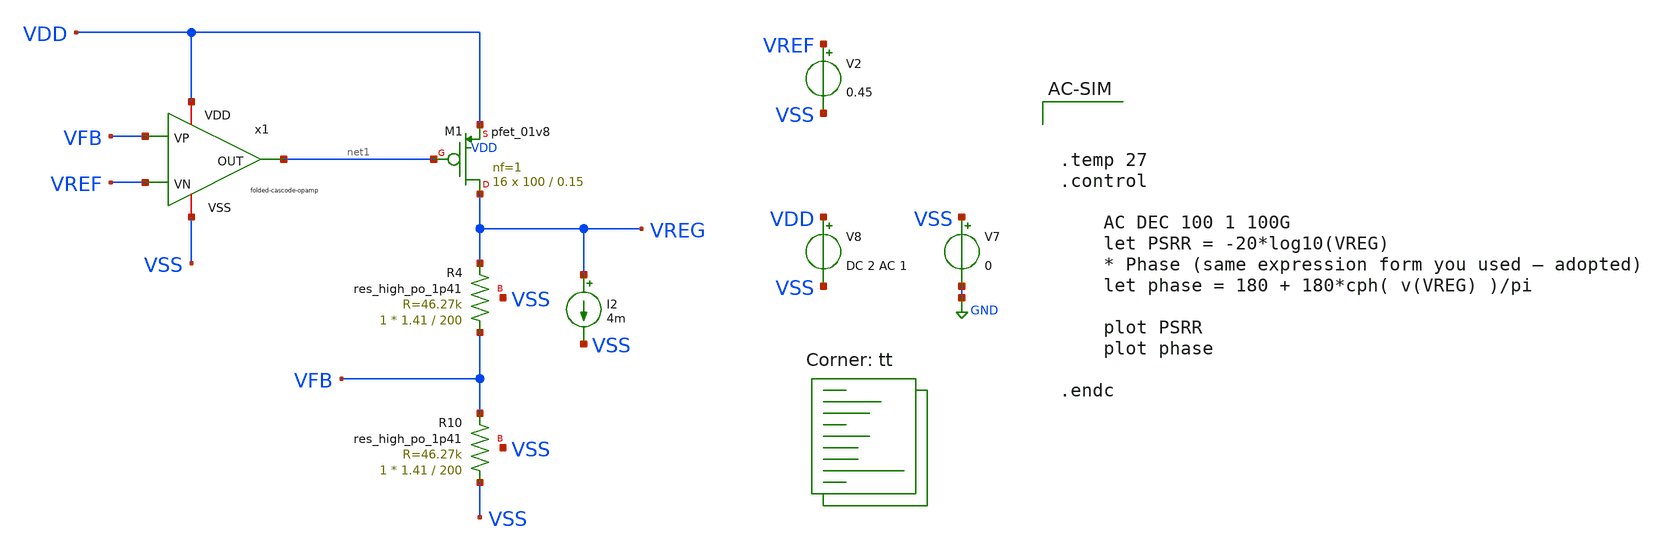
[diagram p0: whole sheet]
** sch_path: pre-regulator.sch
**.subckt pre-regulator
x1 net1 VDD VFB VREF VSS folded-cascode-opamp
XM1 VREG net1 VDD VDD sky130_fd_pr__pfet_01v8 L=0.15 W=100 nf=1 ad='int((nf+1)/2) * W/nf * 0.29' as='int((nf+2)/2) * W/nf * 0.29'
+ pd='2*int((nf+1)/2) * (W/nf + 0.29)' ps='2*int((nf+2)/2) * (W/nf + 0.29)' nrd='0.29 / W' nrs='0.29 / W'
+ sa=0 sb=0 sd=0 mult=16 m=16
XR4 VFB VREG VSS sky130_fd_pr__res_high_po_1p41 L=200 mult=1 m=1
XR10 VSS VFB VSS sky130_fd_pr__res_high_po_1p41 L=200 mult=1 m=1
V2 VREF VSS 0.45
V7 VSS GND 0
V8 VDD VSS DC 2 AC 1
I2 VREG VSS 4m
**** begin user architecture code
.lib $::SKYWATER_MODELS/sky130.lib.spice tt



.temp 27
.control

	AC DEC 100 1 100G
	let PSRR = -20*log10(VREG)
	* Phase (same expression form you used — adopted)
	let phase = 180 + 180*cph( v(VREG) )/pi

	plot PSRR
	plot phase

.endc


**** end user architecture code
**.ends

* expanding   symbol:  afe-icdec-teknofest-2026/bandgap/bgr-opamp2/folded-cascode-opamp.sym # of
*+ pins=5
** sym_path: bandgap/bgr-opamp2/folded-cascode-opamp.sym
** sch_path: bandgap/bgr-opamp2/folded-cascode-opamp.sch
.subckt folded-cascode-opamp OUT VDD VP VN VSS
*.iopin VSS
*.iopin VDD
*.ipin VP
*.ipin VN
*.opin OUT
XR10 VSS net5 VSS sky130_fd_pr__res_high_po_1p41 L=0.235 mult=1 m=1
XM19 net2 net2 VSS GND sky130_fd_pr__nfet_01v8_lvt L=0.5 W=6.4 nf=1 ad='int((nf+1)/2) * W/nf * 0.29'
+ as='int((nf+2)/2) * W/nf * 0.29' pd='2*int((nf+1)/2) * (W/nf + 0.29)' ps='2*int((nf+2)/2) * (W/nf + 0.29)'
+ nrd='0.29 / W' nrs='0.29 / W' sa=0 sb=0 sd=0 mult=1 m=1
XM20 net3 net2 net5 GND sky130_fd_pr__nfet_01v8_lvt L=0.5 W=6.4 nf=1 ad='int((nf+1)/2) * W/nf * 0.29'
+ as='int((nf+2)/2) * W/nf * 0.29' pd='2*int((nf+1)/2) * (W/nf + 0.29)' ps='2*int((nf+2)/2) * (W/nf + 0.29)'
+ nrd='0.29 / W' nrs='0.29 / W' sa=0 sb=0 sd=0 mult=1 m=1
XM16 net4 net1 VDD VDD sky130_fd_pr__pfet_01v8_lvt L=0.5 W=20.8 nf=1 ad='int((nf+1)/2) * W/nf * 0.29'
+ as='int((nf+2)/2) * W/nf * 0.29' pd='2*int((nf+1)/2) * (W/nf + 0.29)' ps='2*int((nf+2)/2) * (W/nf + 0.29)'
+ nrd='0.29 / W' nrs='0.29 / W' sa=0 sb=0 sd=0 mult=1 m=1
XM13 net1 net1 VDD VDD sky130_fd_pr__pfet_01v8_lvt L=0.5 W=20.8 nf=1 ad='int((nf+1)/2) * W/nf * 0.29'
+ as='int((nf+2)/2) * W/nf * 0.29' pd='2*int((nf+1)/2) * (W/nf + 0.29)' ps='2*int((nf+2)/2) * (W/nf + 0.29)'
+ nrd='0.29 / W' nrs='0.29 / W' sa=0 sb=0 sd=0 mult=1 m=1
XM14 net2 net3 net4 VDD sky130_fd_pr__pfet_01v8_lvt L=0.5 W=20.8 nf=1 ad='int((nf+1)/2) * W/nf * 0.29'
+ as='int((nf+2)/2) * W/nf * 0.29' pd='2*int((nf+1)/2) * (W/nf + 0.29)' ps='2*int((nf+2)/2) * (W/nf + 0.29)'
+ nrd='0.29 / W' nrs='0.29 / W' sa=0 sb=0 sd=0 mult=1 m=1
XM17 net3 net3 net1 VDD sky130_fd_pr__pfet_01v8_lvt L=0.5 W=20.8 nf=1 ad='int((nf+1)/2) * W/nf * 0.29'
+ as='int((nf+2)/2) * W/nf * 0.29' pd='2*int((nf+1)/2) * (W/nf + 0.29)' ps='2*int((nf+2)/2) * (W/nf + 0.29)'
+ nrd='0.29 / W' nrs='0.29 / W' sa=0 sb=0 sd=0 mult=1 m=1
XM18 net6 net1 VDD VDD sky130_fd_pr__pfet_01v8_lvt L=0.5 W=20.8 nf=1 ad='int((nf+1)/2) * W/nf * 0.29'
+ as='int((nf+2)/2) * W/nf * 0.29' pd='2*int((nf+1)/2) * (W/nf + 0.29)' ps='2*int((nf+2)/2) * (W/nf + 0.29)'
+ nrd='0.29 / W' nrs='0.29 / W' sa=0 sb=0 sd=0 mult=1 m=1
XM21 net7 net3 net6 VDD sky130_fd_pr__pfet_01v8_lvt L=0.5 W=20.8 nf=1 ad='int((nf+1)/2) * W/nf * 0.29'
+ as='int((nf+2)/2) * W/nf * 0.29' pd='2*int((nf+1)/2) * (W/nf + 0.29)' ps='2*int((nf+2)/2) * (W/nf + 0.29)'
+ nrd='0.29 / W' nrs='0.29 / W' sa=0 sb=0 sd=0 mult=1 m=1
XM22 net7 net7 net9 GND sky130_fd_pr__nfet_01v8_lvt L=0.5 W=1.45 nf=1 ad='int((nf+1)/2) * W/nf * 0.29'
+ as='int((nf+2)/2) * W/nf * 0.29' pd='2*int((nf+1)/2) * (W/nf + 0.29)' ps='2*int((nf+2)/2) * (W/nf + 0.29)'
+ nrd='0.29 / W' nrs='0.29 / W' sa=0 sb=0 sd=0 mult=1 m=1
XM23 net9 net7 net8 GND sky130_fd_pr__nfet_01v8_lvt L=0.5 W=1.45 nf=1 ad='int((nf+1)/2) * W/nf * 0.29'
+ as='int((nf+2)/2) * W/nf * 0.29' pd='2*int((nf+1)/2) * (W/nf + 0.29)' ps='2*int((nf+2)/2) * (W/nf + 0.29)'
+ nrd='0.29 / W' nrs='0.29 / W' sa=0 sb=0 sd=0 mult=1 m=1
XM24 net8 net7 VSS GND sky130_fd_pr__nfet_01v8_lvt L=0.5 W=1.45 nf=1 ad='int((nf+1)/2) * W/nf * 0.29'
+ as='int((nf+2)/2) * W/nf * 0.29' pd='2*int((nf+1)/2) * (W/nf + 0.29)' ps='2*int((nf+2)/2) * (W/nf + 0.29)'
+ nrd='0.29 / W' nrs='0.29 / W' sa=0 sb=0 sd=0 mult=1 m=1
XM26 net16 VN net10 VDD sky130_fd_pr__pfet_01v8_lvt L=1.25 W=84 nf=1 ad='int((nf+1)/2) * W/nf * 0.29'
+ as='int((nf+2)/2) * W/nf * 0.29' pd='2*int((nf+1)/2) * (W/nf + 0.29)' ps='2*int((nf+2)/2) * (W/nf + 0.29)'
+ nrd='0.29 / W' nrs='0.29 / W' sa=0 sb=0 sd=0 mult=1 m=1
XM27 net15 VP net10 VDD sky130_fd_pr__pfet_01v8_lvt L=1.25 W=84 nf=1 ad='int((nf+1)/2) * W/nf * 0.29'
+ as='int((nf+2)/2) * W/nf * 0.29' pd='2*int((nf+1)/2) * (W/nf + 0.29)' ps='2*int((nf+2)/2) * (W/nf + 0.29)'
+ nrd='0.29 / W' nrs='0.29 / W' sa=0 sb=0 sd=0 mult=1 m=1
XM15 net10 OUT VDD VDD sky130_fd_pr__pfet_01v8_lvt L=1.25 W=20.8 nf=1 ad='int((nf+1)/2) * W/nf * 0.29'
+ as='int((nf+2)/2) * W/nf * 0.29' pd='2*int((nf+1)/2) * (W/nf + 0.29)' ps='2*int((nf+2)/2) * (W/nf + 0.29)'
+ nrd='0.29 / W' nrs='0.29 / W' sa=0 sb=0 sd=0 mult=1 m=1
XM25 net12 net1 VDD VDD sky130_fd_pr__pfet_01v8_lvt L=1.25 W=10.4 nf=1 ad='int((nf+1)/2) * W/nf * 0.29'
+ as='int((nf+2)/2) * W/nf * 0.29' pd='2*int((nf+1)/2) * (W/nf + 0.29)' ps='2*int((nf+2)/2) * (W/nf + 0.29)'
+ nrd='0.29 / W' nrs='0.29 / W' sa=0 sb=0 sd=0 mult=1 m=1
XM28 net13 net1 VDD VDD sky130_fd_pr__pfet_01v8_lvt L=1.25 W=10.4 nf=1 ad='int((nf+1)/2) * W/nf * 0.29'
+ as='int((nf+2)/2) * W/nf * 0.29' pd='2*int((nf+1)/2) * (W/nf + 0.29)' ps='2*int((nf+2)/2) * (W/nf + 0.29)'
+ nrd='0.29 / W' nrs='0.29 / W' sa=0 sb=0 sd=0 mult=1 m=1
XM29 net14 net3 net12 VDD sky130_fd_pr__pfet_01v8_lvt L=1.25 W=10.4 nf=1 ad='int((nf+1)/2) * W/nf * 0.29'
+ as='int((nf+2)/2) * W/nf * 0.29' pd='2*int((nf+1)/2) * (W/nf + 0.29)' ps='2*int((nf+2)/2) * (W/nf + 0.29)'
+ nrd='0.29 / W' nrs='0.29 / W' sa=0 sb=0 sd=0 mult=1 m=1
XM30 net11 net3 net13 VDD sky130_fd_pr__pfet_01v8_lvt L=1.25 W=10.4 nf=1 ad='int((nf+1)/2) * W/nf * 0.29'
+ as='int((nf+2)/2) * W/nf * 0.29' pd='2*int((nf+1)/2) * (W/nf + 0.29)' ps='2*int((nf+2)/2) * (W/nf + 0.29)'
+ nrd='0.29 / W' nrs='0.29 / W' sa=0 sb=0 sd=0 mult=1 m=1
XM31 net14 net7 net16 GND sky130_fd_pr__nfet_01v8_lvt L=1.25 W=2.4 nf=1 ad='int((nf+1)/2) * W/nf * 0.29'
+ as='int((nf+2)/2) * W/nf * 0.29' pd='2*int((nf+1)/2) * (W/nf + 0.29)' ps='2*int((nf+2)/2) * (W/nf + 0.29)'
+ nrd='0.29 / W' nrs='0.29 / W' sa=0 sb=0 sd=0 mult=1 m=1
XM32 net11 net7 net15 GND sky130_fd_pr__nfet_01v8_lvt L=1.25 W=2.4 nf=1 ad='int((nf+1)/2) * W/nf * 0.29'
+ as='int((nf+2)/2) * W/nf * 0.29' pd='2*int((nf+1)/2) * (W/nf + 0.29)' ps='2*int((nf+2)/2) * (W/nf + 0.29)'
+ nrd='0.29 / W' nrs='0.29 / W' sa=0 sb=0 sd=0 mult=1 m=1
XM33 net16 net11 VSS GND sky130_fd_pr__nfet_01v8_lvt L=1.25 W=2.4 nf=1 ad='int((nf+1)/2) * W/nf * 0.29'
+ as='int((nf+2)/2) * W/nf * 0.29' pd='2*int((nf+1)/2) * (W/nf + 0.29)' ps='2*int((nf+2)/2) * (W/nf + 0.29)'
+ nrd='0.29 / W' nrs='0.29 / W' sa=0 sb=0 sd=0 mult=1 m=1
XM34 net15 net11 VSS GND sky130_fd_pr__nfet_01v8_lvt L=1.25 W=2.4 nf=1 ad='int((nf+1)/2) * W/nf * 0.29'
+ as='int((nf+2)/2) * W/nf * 0.29' pd='2*int((nf+1)/2) * (W/nf + 0.29)' ps='2*int((nf+2)/2) * (W/nf + 0.29)'
+ nrd='0.29 / W' nrs='0.29 / W' sa=0 sb=0 sd=0 mult=1 m=1
XM35 OUT OUT VDD VDD sky130_fd_pr__pfet_01v8_lvt L=1.25 W=20.8 nf=1 ad='int((nf+1)/2) * W/nf * 0.29'
+ as='int((nf+2)/2) * W/nf * 0.29' pd='2*int((nf+1)/2) * (W/nf + 0.29)' ps='2*int((nf+2)/2) * (W/nf + 0.29)'
+ nrd='0.29 / W' nrs='0.29 / W' sa=0 sb=0 sd=0 mult=1 m=1
XM1 OUT net14 VSS GND sky130_fd_pr__nfet_01v8_lvt L=1.25 W=2.5 nf=1 ad='int((nf+1)/2) * W/nf * 0.29'
+ as='int((nf+2)/2) * W/nf * 0.29' pd='2*int((nf+1)/2) * (W/nf + 0.29)' ps='2*int((nf+2)/2) * (W/nf + 0.29)'
+ nrd='0.29 / W' nrs='0.29 / W' sa=0 sb=0 sd=0 mult=1 m=1
XC1 OUT net14 sky130_fd_pr__cap_mim_m3_1 W=25 L=25 MF=2 m=2
.ends

.GLOBAL GND
.end
